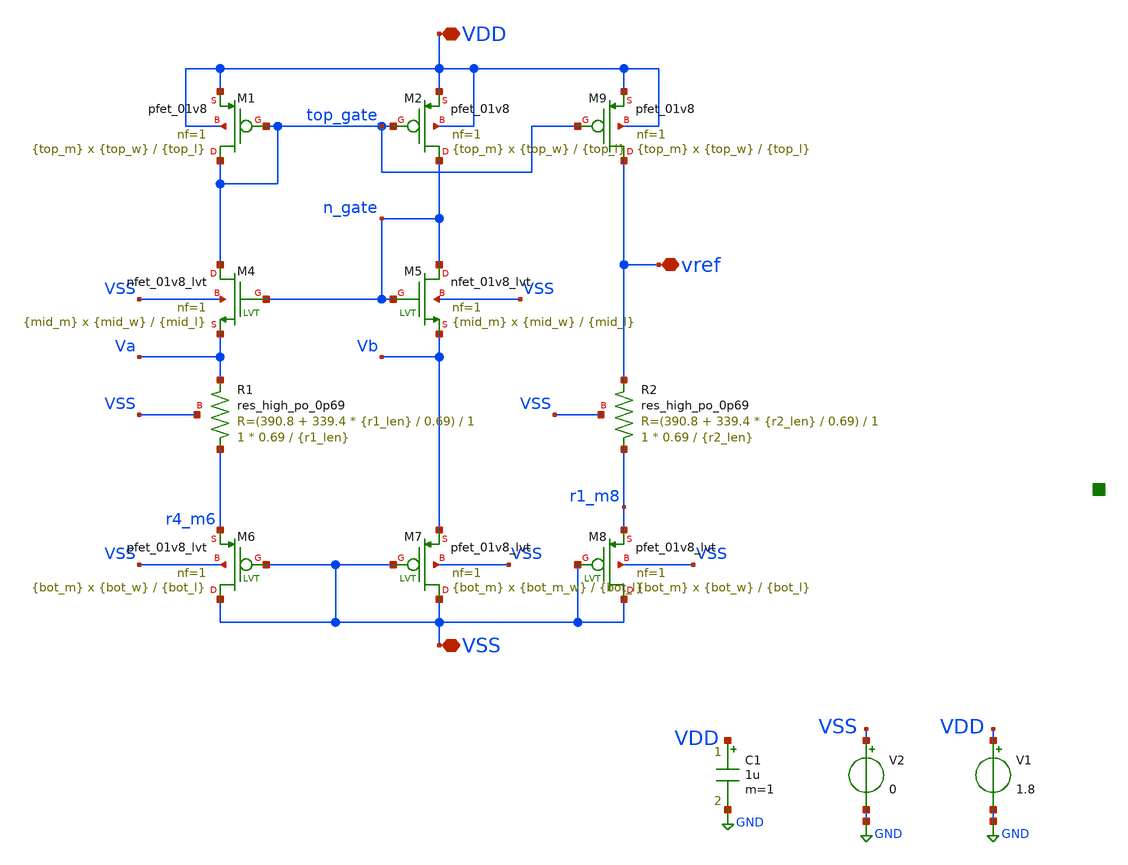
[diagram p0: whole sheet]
** sch_path: xschem/bandgap-op-dtmos.sch
**.subckt bandgap-op-dtmos VSS VDD vref
*.iopin VSS
*.iopin VDD
*.iopin vref
XR1 r4_m6 Va VSS sky130_fd_pr__res_high_po_0p69 L={r1_len} mult=1 m=1
XR2 r1_m8 vref VSS sky130_fd_pr__res_high_po_0p69 L={r2_len} mult=1 m=1
V1 VDD GND 1.8
V2 VSS GND 0
C1 VDD GND 1u m=1
XM5 n_gate n_gate Vb VSS sky130_fd_pr__nfet_01v8_lvt L={mid_l} W={mid_w} nf=1 ad='int((nf+1)/2) * W/nf * 0.29'
+ as='int((nf+2)/2) * W/nf * 0.29' pd='2*int((nf+1)/2) * (W/nf + 0.29)' ps='2*int((nf+2)/2) * (W/nf + 0.29)'
+ nrd='0.29 / W' nrs='0.29 / W' sa=0 sb=0 sd=0 mult={mid_m} m={mid_m}
XM4 top_gate n_gate Va VSS sky130_fd_pr__nfet_01v8_lvt L={mid_l} W={mid_w} nf=1 ad='int((nf+1)/2) * W/nf * 0.29'
+ as='int((nf+2)/2) * W/nf * 0.29' pd='2*int((nf+1)/2) * (W/nf + 0.29)' ps='2*int((nf+2)/2) * (W/nf + 0.29)'
+ nrd='0.29 / W' nrs='0.29 / W' sa=0 sb=0 sd=0 mult={mid_m} m={mid_m}
XM6 VSS VSS r4_m6 VSS sky130_fd_pr__pfet_01v8_lvt L={bot_l} W={bot_w} nf=1 ad='int((nf+1)/2) * W/nf * 0.29'
+ as='int((nf+2)/2) * W/nf * 0.29' pd='2*int((nf+1)/2) * (W/nf + 0.29)' ps='2*int((nf+2)/2) * (W/nf + 0.29)'
+ nrd='0.29 / W' nrs='0.29 / W' sa=0 sb=0 sd=0 mult={bot_m} m={bot_m}
XM8 VSS VSS r1_m8 VSS sky130_fd_pr__pfet_01v8_lvt L={bot_l} W={bot_w} nf=1 ad='int((nf+1)/2) * W/nf * 0.29'
+ as='int((nf+2)/2) * W/nf * 0.29' pd='2*int((nf+1)/2) * (W/nf + 0.29)' ps='2*int((nf+2)/2) * (W/nf + 0.29)'
+ nrd='0.29 / W' nrs='0.29 / W' sa=0 sb=0 sd=0 mult={bot_m} m={bot_m}
XM7 VSS VSS Vb VSS sky130_fd_pr__pfet_01v8_lvt L={bot_l} W={bot_m_w} nf=1 ad='int((nf+1)/2) * W/nf * 0.29'
+ as='int((nf+2)/2) * W/nf * 0.29' pd='2*int((nf+1)/2) * (W/nf + 0.29)' ps='2*int((nf+2)/2) * (W/nf + 0.29)'
+ nrd='0.29 / W' nrs='0.29 / W' sa=0 sb=0 sd=0 mult={bot_m} m={bot_m}
XM9 vref top_gate VDD VDD sky130_fd_pr__pfet_01v8 L={top_l} W={top_w} nf=1 ad='int((nf+1)/2) * W/nf * 0.29'
+ as='int((nf+2)/2) * W/nf * 0.29' pd='2*int((nf+1)/2) * (W/nf + 0.29)' ps='2*int((nf+2)/2) * (W/nf + 0.29)'
+ nrd='0.29 / W' nrs='0.29 / W' sa=0 sb=0 sd=0 mult={top_m} m={top_m}
XM1 top_gate top_gate VDD VDD sky130_fd_pr__pfet_01v8 L={top_l} W={top_w} nf=1 ad='int((nf+1)/2) * W/nf * 0.29'
+ as='int((nf+2)/2) * W/nf * 0.29' pd='2*int((nf+1)/2) * (W/nf + 0.29)' ps='2*int((nf+2)/2) * (W/nf + 0.29)'
+ nrd='0.29 / W' nrs='0.29 / W' sa=0 sb=0 sd=0 mult={top_m} m={top_m}
XM2 n_gate top_gate VDD VDD sky130_fd_pr__pfet_01v8 L={top_l} W={top_w} nf=1 ad='int((nf+1)/2) * W/nf * 0.29'
+ as='int((nf+2)/2) * W/nf * 0.29' pd='2*int((nf+1)/2) * (W/nf + 0.29)' ps='2*int((nf+2)/2) * (W/nf + 0.29)'
+ nrd='0.29 / W' nrs='0.29 / W' sa=0 sb=0 sd=0 mult={top_m} m={top_m}
**** begin user architecture code

** opencircuitdesign pdks install
.lib $::SKYWATER_MODELS/sky130.lib.spice tt





.param top_l = 10
.param top_w = 10
.param top_m = 1

.param mid_l = 5
.param mid_w = 10
.param mid_m = 1

.param bot_l = 2
.param bot_w = 10
.param bot_m_w = 2
.param bot_m = 1
.param r1_len = 100
.param r2_len = 100


.control

let do_op = 0
let do_dc = 1
let do_loop_temp = 0

* operating point
if (do_op)
  op
  write bandgap-op-dtmos.raw
endif

* dc & temp sweep
if (do_dc)
  dc v1 1.3 2 0.01
  write bandgap-op-dtmos.raw
  set appendwrite
  reset
  dc temp 10 100 1
  write bandgap-op-dtmos.raw

endif

* temp sweep while changing a value
if (do_loop_temp)
  let bot_m_w_val = 2
  repeat 20
    alterparam bot_m_w = $&bot_m_w_val
    let bot_m_w_val = bot_m_w_val + 0.1

    dc temp 10 100 1
    write bandgap-op-dtmos.raw
    set appendwrite
    reset
  end
endif

*quit
.endc


**** end user architecture code
**.ends
.GLOBAL GND
.end
